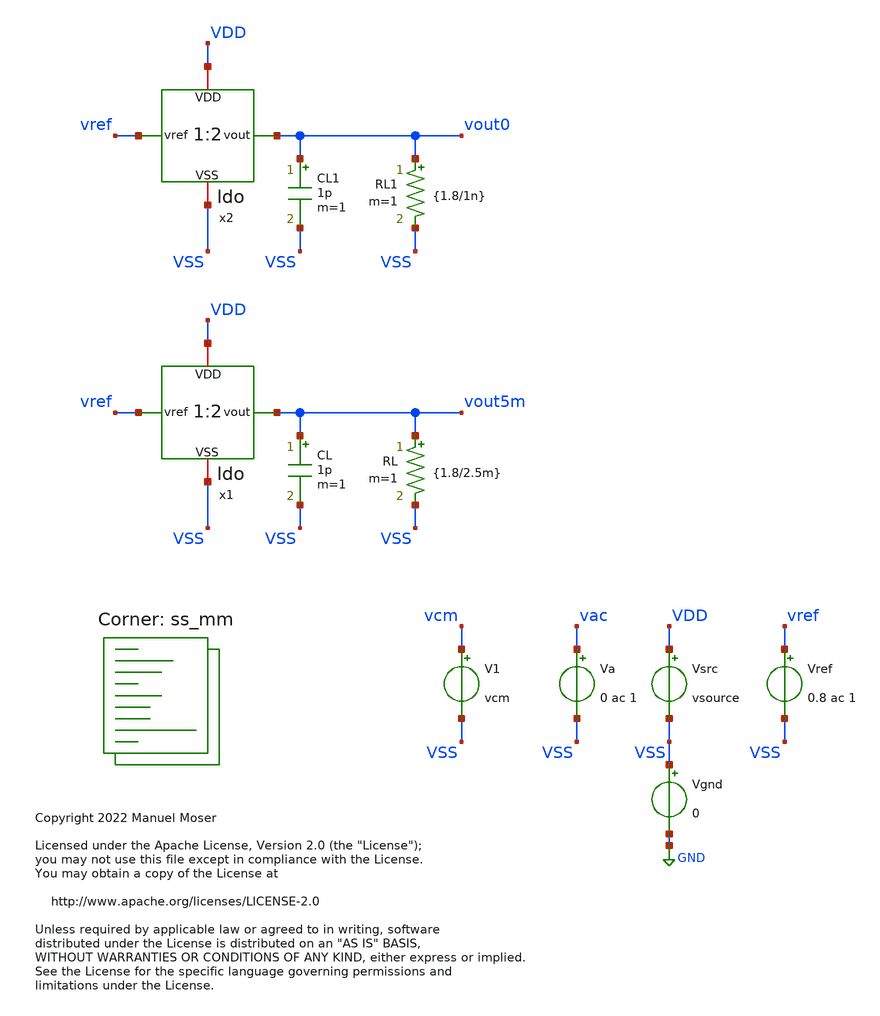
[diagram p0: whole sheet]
** sch_path: xschem/ldo_tb.sch
* Copyright 2022 Manuel Moser
* Licensed under the Apache License, Version 2.0 (the "License");
**.subckt ldo_tb
V1 vcm VSS vcm
Vref vref VSS 0.8 ac 1
Vsrc VDD VSS vsource
Vgnd VSS GND 0
Va vac VSS 0 ac 1
CL vout5m VSS 1p m=1
RL vout5m VSS {1.8/2.5m} m=1
x1 VDD vref vout5m VSS ldo
CL1 vout0 VSS 1p m=1
x2 VDD vref vout0 VSS ldo
RL1 vout0 VSS {1.8/1n} m=1
**** begin user architecture code



.temp 27
.options savecurrents
.option gmin = 1e-18
.option RSHUNT=1E20

.param vsource = 1.8
.param vcm = {vsource/2}


.save all
.control
set num_threads = 12
write results_ldo.raw
set appendwrite

repeat 20
 reset

dc vref 0 1 0.01 temp -30 60 90
write results_ldo.raw vout5m vout0 x1.vota x1.vfb @m.x1.xm5.msky130_fd_pr__nfet_01v8_lvt[id] i(vsrc)

ac dec 10 1 10meg
write results_ldo.raw vout5m


end

.endc




.lib $::SKYWATER_MODELS/sky130.lib.spice ss_mm
**** end user architecture code
**.ends

* expanding   symbol:  ldo.sym # of pins=4
** sym_path: xschem/ldo.sym
** sch_path: xschem/ldo.sch
.subckt ldo VDD vref vout VSS
*.ipin vref
*.iopin VDD
*.iopin VSS
*.opin vout
x1 VDD vref vota vfb VSS ldo_ota
XM1 vout vota VDD VDD sky130_fd_pr__pfet_01v8_hvt L=0.15 W='5 * 10 ' nf=10 ad='int((nf+1)/2) * W / nf * 0.29'
+ as='int((nf+2)/2) * W / nf * 0.29' pd='2*int((nf+1)/2) * (W / nf + 0.29)' ps='2*int((nf+2)/2) * (W / nf + 0.29)'
+ nrd='0.29 / W ' nrs='0.29 / W ' sa=0 sb=0 sd=0 mult=9 m=9
XM5 vout vout net1 net1 sky130_fd_pr__nfet_01v8_lvt L=4 W='2 * 2 ' nf=2 ad='int((nf+1)/2) * W/nf * 0.29'
+ as='int((nf+2)/2) * W/nf * 0.29' pd='2*int((nf+1)/2) * (W/nf + 0.29)' ps='2*int((nf+2)/2) * (W/nf + 0.29)'
+ nrd='0.29 / W' nrs='0.29 / W' sa=0 sb=0 sd=0 mult=1 m=1
XM2 net1 net1 vfb vfb sky130_fd_pr__nfet_01v8_lvt L=4 W='2 * 2 ' nf=2 ad='int((nf+1)/2) * W/nf * 0.29'
+ as='int((nf+2)/2) * W/nf * 0.29' pd='2*int((nf+1)/2) * (W/nf + 0.29)' ps='2*int((nf+2)/2) * (W/nf + 0.29)'
+ nrd='0.29 / W' nrs='0.29 / W' sa=0 sb=0 sd=0 mult=1 m=1
XM3 vfb vfb net2 net2 sky130_fd_pr__nfet_01v8_lvt L=4 W='2 * 2 ' nf=2 ad='int((nf+1)/2) * W/nf * 0.29'
+ as='int((nf+2)/2) * W/nf * 0.29' pd='2*int((nf+1)/2) * (W/nf + 0.29)' ps='2*int((nf+2)/2) * (W/nf + 0.29)'
+ nrd='0.29 / W' nrs='0.29 / W' sa=0 sb=0 sd=0 mult=1 m=1
XM6 net2 net2 VSS VSS sky130_fd_pr__nfet_01v8_lvt L=4 W='2 * 2 ' nf=2 ad='int((nf+1)/2) * W/nf * 0.29'
+ as='int((nf+2)/2) * W/nf * 0.29' pd='2*int((nf+1)/2) * (W/nf + 0.29)' ps='2*int((nf+2)/2) * (W/nf + 0.29)'
+ nrd='0.29 / W' nrs='0.29 / W' sa=0 sb=0 sd=0 mult=1 m=1
.ends


* expanding   symbol:  ldo_ota.sym # of pins=5
** sym_path: xschem/ldo_ota.sym
** sch_path: xschem/ldo_ota.sch
.subckt ldo_ota VDD inp outn inn VSS
*.iopin VDD
*.iopin VSS
*.ipin inp
*.ipin inn
*.opin outn
x2 bias2 VDD VSS bias1 ldo_isource
XM10 net1 bias2 VDD VDD sky130_fd_pr__pfet_01v8_lvt L=8 W='1 * 1 ' nf=1 ad='int((nf+1)/2) * W / nf * 0.29'
+ as='int((nf+2)/2) * W / nf * 0.29' pd='2*int((nf+1)/2) * (W / nf + 0.29)' ps='2*int((nf+2)/2) * (W / nf + 0.29)'
+ nrd='0.29 / W ' nrs='0.29 / W ' sa=0 sb=0 sd=0 mult=1 m=1
XM12 bias2 bias2 net1 VDD sky130_fd_pr__pfet_01v8_lvt L=1 W='3 * 9 ' nf=9 ad='int((nf+1)/2) * W / nf * 0.29'
+ as='int((nf+2)/2) * W / nf * 0.29' pd='2*int((nf+1)/2) * (W / nf + 0.29)' ps='2*int((nf+2)/2) * (W / nf + 0.29)'
+ nrd='0.29 / W ' nrs='0.29 / W ' sa=0 sb=0 sd=0 mult=1 m=1
XM1 net2 bias1 VDD VDD sky130_fd_pr__pfet_01v8_lvt L=8 W='1 * 3 ' nf=3 ad='int((nf+1)/2) * W / nf * 0.29'
+ as='int((nf+2)/2) * W / nf * 0.29' pd='2*int((nf+1)/2) * (W / nf + 0.29)' ps='2*int((nf+2)/2) * (W / nf + 0.29)'
+ nrd='0.29 / W ' nrs='0.29 / W ' sa=0 sb=0 sd=0 mult=1 m=1
XM2 bias1 bias2 net2 VDD sky130_fd_pr__pfet_01v8_lvt L=1 W='3 * 9 ' nf=9 ad='int((nf+1)/2) * W / nf * 0.29'
+ as='int((nf+2)/2) * W / nf * 0.29' pd='2*int((nf+1)/2) * (W / nf + 0.29)' ps='2*int((nf+2)/2) * (W / nf + 0.29)'
+ nrd='0.29 / W ' nrs='0.29 / W ' sa=0 sb=0 sd=0 mult=1 m=1
XM3 net3 bias1 VDD VDD sky130_fd_pr__pfet_01v8_lvt L=8 W='1 * 3 ' nf=3 ad='int((nf+1)/2) * W / nf * 0.29'
+ as='int((nf+2)/2) * W / nf * 0.29' pd='2*int((nf+1)/2) * (W / nf + 0.29)' ps='2*int((nf+2)/2) * (W / nf + 0.29)'
+ nrd='0.29 / W ' nrs='0.29 / W ' sa=0 sb=0 sd=0 mult=1 m=1
XM4 bias3 bias2 net3 VDD sky130_fd_pr__pfet_01v8_lvt L=1 W='3 * 9 ' nf=9 ad='int((nf+1)/2) * W / nf * 0.29'
+ as='int((nf+2)/2) * W / nf * 0.29' pd='2*int((nf+1)/2) * (W / nf + 0.29)' ps='2*int((nf+2)/2) * (W / nf + 0.29)'
+ nrd='0.29 / W ' nrs='0.29 / W ' sa=0 sb=0 sd=0 mult=1 m=1
XM5 net4 bias1 VDD VDD sky130_fd_pr__pfet_01v8_lvt L=8 W='1 * 3 ' nf=3 ad='int((nf+1)/2) * W / nf * 0.29'
+ as='int((nf+2)/2) * W / nf * 0.29' pd='2*int((nf+1)/2) * (W / nf + 0.29)' ps='2*int((nf+2)/2) * (W / nf + 0.29)'
+ nrd='0.29 / W ' nrs='0.29 / W ' sa=0 sb=0 sd=0 mult=1 m=1
XM8 bias4 bias2 net4 VDD sky130_fd_pr__pfet_01v8_lvt L=1 W='3 * 9 ' nf=9 ad='int((nf+1)/2) * W / nf * 0.29'
+ as='int((nf+2)/2) * W / nf * 0.29' pd='2*int((nf+1)/2) * (W / nf + 0.29)' ps='2*int((nf+2)/2) * (W / nf + 0.29)'
+ nrd='0.29 / W ' nrs='0.29 / W ' sa=0 sb=0 sd=0 mult=1 m=1
XM9 bias3 bias3 net5 VSS sky130_fd_pr__nfet_01v8_lvt L=4 W='1 * 9 ' nf=9 ad='int((nf+1)/2) * W / nf * 0.29'
+ as='int((nf+2)/2) * W / nf * 0.29' pd='2*int((nf+1)/2) * (W / nf + 0.29)' ps='2*int((nf+2)/2) * (W / nf + 0.29)'
+ nrd='0.29 / W ' nrs='0.29 / W ' sa=0 sb=0 sd=0 mult=1 m=1
XM11 net5 bias3 net10 VSS sky130_fd_pr__nfet_01v8_lvt L=4 W='1 * 1 ' nf=1 ad='int((nf+1)/2) * W / nf * 0.29'
+ as='int((nf+2)/2) * W / nf * 0.29' pd='2*int((nf+1)/2) * (W / nf + 0.29)' ps='2*int((nf+2)/2) * (W / nf + 0.29)'
+ nrd='0.29 / W ' nrs='0.29 / W ' sa=0 sb=0 sd=0 mult=1 m=1
XM13 bias4 bias3 net6 VSS sky130_fd_pr__nfet_01v8_lvt L=4 W='1 * 9 ' nf=9 ad='int((nf+1)/2) * W / nf * 0.29'
+ as='int((nf+2)/2) * W / nf * 0.29' pd='2*int((nf+1)/2) * (W / nf + 0.29)' ps='2*int((nf+2)/2) * (W / nf + 0.29)'
+ nrd='0.29 / W ' nrs='0.29 / W ' sa=0 sb=0 sd=0 mult=1 m=1
XM14 net6 bias4 net7 VSS sky130_fd_pr__nfet_01v8_lvt L=4 W='1 * 3 ' nf=3 ad='int((nf+1)/2) * W / nf * 0.29'
+ as='int((nf+2)/2) * W / nf * 0.29' pd='2*int((nf+1)/2) * (W / nf + 0.29)' ps='2*int((nf+2)/2) * (W / nf + 0.29)'
+ nrd='0.29 / W ' nrs='0.29 / W ' sa=0 sb=0 sd=0 mult=1 m=1
XM6 net7 bias4 net8 VSS sky130_fd_pr__nfet_01v8_lvt L=4 W='1 * 3 ' nf=3 ad='int((nf+1)/2) * W / nf * 0.29'
+ as='int((nf+2)/2) * W / nf * 0.29' pd='2*int((nf+1)/2) * (W / nf + 0.29)' ps='2*int((nf+2)/2) * (W / nf + 0.29)'
+ nrd='0.29 / W ' nrs='0.29 / W ' sa=0 sb=0 sd=0 mult=1 m=1
XM7 net10 bias3 net9 VSS sky130_fd_pr__nfet_01v8_lvt L=4 W='1 * 1 ' nf=1 ad='int((nf+1)/2) * W / nf * 0.29'
+ as='int((nf+2)/2) * W / nf * 0.29' pd='2*int((nf+1)/2) * (W / nf + 0.29)' ps='2*int((nf+2)/2) * (W / nf + 0.29)'
+ nrd='0.29 / W ' nrs='0.29 / W ' sa=0 sb=0 sd=0 mult=1 m=1
XM15 net8 bias4 VSS VSS sky130_fd_pr__nfet_01v8_lvt L=4 W='1 * 3 ' nf=3 ad='int((nf+1)/2) * W / nf * 0.29'
+ as='int((nf+2)/2) * W / nf * 0.29' pd='2*int((nf+1)/2) * (W / nf + 0.29)' ps='2*int((nf+2)/2) * (W / nf + 0.29)'
+ nrd='0.29 / W ' nrs='0.29 / W ' sa=0 sb=0 sd=0 mult=1 m=1
XM16 net9 bias3 VSS VSS sky130_fd_pr__nfet_01v8_lvt L=4 W='1 * 1 ' nf=1 ad='int((nf+1)/2) * W / nf * 0.29'
+ as='int((nf+2)/2) * W / nf * 0.29' pd='2*int((nf+1)/2) * (W / nf + 0.29)' ps='2*int((nf+2)/2) * (W / nf + 0.29)'
+ nrd='0.29 / W ' nrs='0.29 / W ' sa=0 sb=0 sd=0 mult=1 m=1
x1 VDD inp inn bias1 bias2 bias3 outn VSS bias4 ldo_fc_n
.ends


* expanding   symbol:  ldo_isource.sym # of pins=4
** sym_path: xschem/ldo_isource.sym
** sch_path: xschem/ldo_isource.sch
.subckt ldo_isource curr_n1 VDD VSS curr_n2
*.iopin VDD
*.iopin VSS
*.ipin curr_n1
*.ipin curr_n2
XMP2 VGP VGP net4 VDD sky130_fd_pr__pfet_01v8_lvt L=8 W='0.55 * 7 ' nf=7 ad='int((nf+1)/2) * W / nf * 0.29'
+ as='int((nf+2)/2) * W / nf * 0.29' pd='2*int((nf+1)/2) * (W / nf + 0.29)' ps='2*int((nf+2)/2) * (W / nf + 0.29)'
+ nrd='0.29 / W ' nrs='0.29 / W ' sa=0 sb=0 sd=0 mult=1 m=1
XMP1 VGN VGP net3 VDD sky130_fd_pr__pfet_01v8_lvt L=8 W='0.55 * 7 ' nf=7 ad='int((nf+1)/2) * W / nf * 0.29'
+ as='int((nf+2)/2) * W / nf * 0.29' pd='2*int((nf+1)/2) * (W / nf + 0.29)' ps='2*int((nf+2)/2) * (W / nf + 0.29)'
+ nrd='0.29 / W ' nrs='0.29 / W ' sa=0 sb=0 sd=0 mult=1 m=1
XMN1 VGN VGN net1 VSS sky130_fd_pr__nfet_01v8_lvt L=8 W='7 * 1 ' nf=1 ad='int((nf+1)/2) * W / nf * 0.29'
+ as='int((nf+2)/2) * W / nf * 0.29' pd='2*int((nf+1)/2) * (W / nf + 0.29)' ps='2*int((nf+2)/2) * (W / nf + 0.29)'
+ nrd='0.29 / W ' nrs='0.29 / W ' sa=0 sb=0 sd=0 mult=1 m=1
XMN2 VGP VGN net2 VSS sky130_fd_pr__nfet_01v8_lvt L=8 W='7 * 1 ' nf=1 ad='int((nf+1)/2) * W / nf * 0.29'
+ as='int((nf+2)/2) * W / nf * 0.29' pd='2*int((nf+1)/2) * (W / nf + 0.29)' ps='2*int((nf+2)/2) * (W / nf + 0.29)'
+ nrd='0.29 / W ' nrs='0.29 / W ' sa=0 sb=0 sd=0 mult=5 m=5
XMN3 net1 VGN VSS VSS sky130_fd_pr__nfet_01v8_lvt L=8 W='7 * 1 ' nf=1 ad='int((nf+1)/2) * W / nf * 0.29'
+ as='int((nf+2)/2) * W / nf * 0.29' pd='2*int((nf+1)/2) * (W / nf + 0.29)' ps='2*int((nf+2)/2) * (W / nf + 0.29)'
+ nrd='0.29 / W ' nrs='0.29 / W ' sa=0 sb=0 sd=0 mult=1 m=1
XMN4 net2 VGN Vref VSS sky130_fd_pr__nfet_01v8_lvt L=8 W='7 * 1 ' nf=1 ad='int((nf+1)/2) * W / nf * 0.29'
+ as='int((nf+2)/2) * W / nf * 0.29' pd='2*int((nf+1)/2) * (W / nf + 0.29)' ps='2*int((nf+2)/2) * (W / nf + 0.29)'
+ nrd='0.29 / W ' nrs='0.29 / W ' sa=0 sb=0 sd=0 mult=5 m=5
XMP4 net3 VGP VDD VDD sky130_fd_pr__pfet_01v8_lvt L=8 W='0.55 * 7 ' nf=7 ad='int((nf+1)/2) * W / nf * 0.29'
+ as='int((nf+2)/2) * W / nf * 0.29' pd='2*int((nf+1)/2) * (W / nf + 0.29)' ps='2*int((nf+2)/2) * (W / nf + 0.29)'
+ nrd='0.29 / W ' nrs='0.29 / W ' sa=0 sb=0 sd=0 mult=1 m=1
XMP5 net4 VGP VDD VDD sky130_fd_pr__pfet_01v8_lvt L=8 W='0.55 * 7 ' nf=7 ad='int((nf+1)/2) * W / nf * 0.29'
+ as='int((nf+2)/2) * W / nf * 0.29' pd='2*int((nf+1)/2) * (W / nf + 0.29)' ps='2*int((nf+2)/2) * (W / nf + 0.29)'
+ nrd='0.29 / W ' nrs='0.29 / W ' sa=0 sb=0 sd=0 mult=1 m=1
XMP3 Vrefgate VGP net19 VDD sky130_fd_pr__pfet_01v8_lvt L=8 W='0.55 * 7 ' nf=7 ad='int((nf+1)/2) * W / nf * 0.29'
+ as='int((nf+2)/2) * W / nf * 0.29' pd='2*int((nf+1)/2) * (W / nf + 0.29)' ps='2*int((nf+2)/2) * (W / nf + 0.29)'
+ nrd='0.29 / W ' nrs='0.29 / W ' sa=0 sb=0 sd=0 mult=1 m=1
XM2 net5 Vrefgate net6 VSS sky130_fd_pr__nfet_01v8 L=4 W='1 * 1 ' nf=1 ad='int((nf+1)/2) * W / nf * 0.29'
+ as='int((nf+2)/2) * W / nf * 0.29' pd='2*int((nf+1)/2) * (W / nf + 0.29)' ps='2*int((nf+2)/2) * (W / nf + 0.29)'
+ nrd='0.29 / W ' nrs='0.29 / W ' sa=0 sb=0 sd=0 mult=1 m=1
XM3 net8 Vrefgate VSS VSS sky130_fd_pr__nfet_01v8 L=4 W='1 * 1 ' nf=1 ad='int((nf+1)/2) * W / nf * 0.29'
+ as='int((nf+2)/2) * W / nf * 0.29' pd='2*int((nf+1)/2) * (W / nf + 0.29)' ps='2*int((nf+2)/2) * (W / nf + 0.29)'
+ nrd='0.29 / W ' nrs='0.29 / W ' sa=0 sb=0 sd=0 mult=1 m=1
XM1 net7 Vrefgate net8 VSS sky130_fd_pr__nfet_01v8 L=4 W='1 * 1 ' nf=1 ad='int((nf+1)/2) * W / nf * 0.29'
+ as='int((nf+2)/2) * W / nf * 0.29' pd='2*int((nf+1)/2) * (W / nf + 0.29)' ps='2*int((nf+2)/2) * (W / nf + 0.29)'
+ nrd='0.29 / W ' nrs='0.29 / W ' sa=0 sb=0 sd=0 mult=1 m=1
XM4 net6 Vrefgate net7 VSS sky130_fd_pr__nfet_01v8 L=4 W='1 * 1 ' nf=1 ad='int((nf+1)/2) * W / nf * 0.29'
+ as='int((nf+2)/2) * W / nf * 0.29' pd='2*int((nf+1)/2) * (W / nf + 0.29)' ps='2*int((nf+2)/2) * (W / nf + 0.29)'
+ nrd='0.29 / W ' nrs='0.29 / W ' sa=0 sb=0 sd=0 mult=1 m=1
XMN5 net10 Vrefgate VSS VSS sky130_fd_pr__nfet_01v8_lvt L=4 W='1 * 1 ' nf=1 ad='int((nf+1)/2) * W / nf * 0.29'
+ as='int((nf+2)/2) * W / nf * 0.29' pd='2*int((nf+1)/2) * (W / nf + 0.29)' ps='2*int((nf+2)/2) * (W / nf + 0.29)'
+ nrd='0.29 / W ' nrs='0.29 / W ' sa=0 sb=0 sd=0 mult=1 m=1
XMN6 net14 Vrefgate net9 VSS sky130_fd_pr__nfet_01v8_lvt L=4 W='1 * 1 ' nf=1 ad='int((nf+1)/2) * W / nf * 0.29'
+ as='int((nf+2)/2) * W / nf * 0.29' pd='2*int((nf+1)/2) * (W / nf + 0.29)' ps='2*int((nf+2)/2) * (W / nf + 0.29)'
+ nrd='0.29 / W ' nrs='0.29 / W ' sa=0 sb=0 sd=0 mult=1 m=1
XMN9 net16 Vrefgate net14 VSS sky130_fd_pr__nfet_01v8_lvt L=4 W='1 * 1 ' nf=1 ad='int((nf+1)/2) * W / nf * 0.29'
+ as='int((nf+2)/2) * W / nf * 0.29' pd='2*int((nf+1)/2) * (W / nf + 0.29)' ps='2*int((nf+2)/2) * (W / nf + 0.29)'
+ nrd='0.29 / W ' nrs='0.29 / W ' sa=0 sb=0 sd=0 mult=1 m=1
XM5 Vrefgate Vrefgate net5 VSS sky130_fd_pr__nfet_01v8 L=4 W='1 * 1 ' nf=1 ad='int((nf+1)/2) * W / nf * 0.29'
+ as='int((nf+2)/2) * W / nf * 0.29' pd='2*int((nf+1)/2) * (W / nf + 0.29)' ps='2*int((nf+2)/2) * (W / nf + 0.29)'
+ nrd='0.29 / W ' nrs='0.29 / W ' sa=0 sb=0 sd=0 mult=1 m=1
XMN10 net11 Vrefgate net10 VSS sky130_fd_pr__nfet_01v8_lvt L=4 W='1 * 1 ' nf=1 ad='int((nf+1)/2) * W / nf * 0.29'
+ as='int((nf+2)/2) * W / nf * 0.29' pd='2*int((nf+1)/2) * (W / nf + 0.29)' ps='2*int((nf+2)/2) * (W / nf + 0.29)'
+ nrd='0.29 / W ' nrs='0.29 / W ' sa=0 sb=0 sd=0 mult=1 m=1
XMN11 net12 Vrefgate net11 VSS sky130_fd_pr__nfet_01v8_lvt L=4 W='1 * 1 ' nf=1 ad='int((nf+1)/2) * W / nf * 0.29'
+ as='int((nf+2)/2) * W / nf * 0.29' pd='2*int((nf+1)/2) * (W / nf + 0.29)' ps='2*int((nf+2)/2) * (W / nf + 0.29)'
+ nrd='0.29 / W ' nrs='0.29 / W ' sa=0 sb=0 sd=0 mult=1 m=1
XMN12 net13 Vrefgate net12 VSS sky130_fd_pr__nfet_01v8_lvt L=4 W='1 * 1 ' nf=1 ad='int((nf+1)/2) * W / nf * 0.29'
+ as='int((nf+2)/2) * W / nf * 0.29' pd='2*int((nf+1)/2) * (W / nf + 0.29)' ps='2*int((nf+2)/2) * (W / nf + 0.29)'
+ nrd='0.29 / W ' nrs='0.29 / W ' sa=0 sb=0 sd=0 mult=1 m=1
XMN13 net9 Vrefgate net13 VSS sky130_fd_pr__nfet_01v8_lvt L=4 W='1 * 1 ' nf=1 ad='int((nf+1)/2) * W / nf * 0.29'
+ as='int((nf+2)/2) * W / nf * 0.29' pd='2*int((nf+1)/2) * (W / nf + 0.29)' ps='2*int((nf+2)/2) * (W / nf + 0.29)'
+ nrd='0.29 / W ' nrs='0.29 / W ' sa=0 sb=0 sd=0 mult=1 m=1
XMN7 net18 Vrefgate net15 VSS sky130_fd_pr__nfet_01v8_lvt L=4 W='1 * 1 ' nf=1 ad='int((nf+1)/2) * W / nf * 0.29'
+ as='int((nf+2)/2) * W / nf * 0.29' pd='2*int((nf+1)/2) * (W / nf + 0.29)' ps='2*int((nf+2)/2) * (W / nf + 0.29)'
+ nrd='0.29 / W ' nrs='0.29 / W ' sa=0 sb=0 sd=0 mult=1 m=1
XMN8 Vref Vrefgate net18 VSS sky130_fd_pr__nfet_01v8_lvt L=4 W='1 * 1 ' nf=1 ad='int((nf+1)/2) * W / nf * 0.29'
+ as='int((nf+2)/2) * W / nf * 0.29' pd='2*int((nf+1)/2) * (W / nf + 0.29)' ps='2*int((nf+2)/2) * (W / nf + 0.29)'
+ nrd='0.29 / W ' nrs='0.29 / W ' sa=0 sb=0 sd=0 mult=1 m=1
XMN14 net17 Vrefgate net16 VSS sky130_fd_pr__nfet_01v8_lvt L=4 W='1 * 1 ' nf=1 ad='int((nf+1)/2) * W / nf * 0.29'
+ as='int((nf+2)/2) * W / nf * 0.29' pd='2*int((nf+1)/2) * (W / nf + 0.29)' ps='2*int((nf+2)/2) * (W / nf + 0.29)'
+ nrd='0.29 / W ' nrs='0.29 / W ' sa=0 sb=0 sd=0 mult=1 m=1
XMN15 net15 Vrefgate net17 VSS sky130_fd_pr__nfet_01v8_lvt L=4 W='1 * 1 ' nf=1 ad='int((nf+1)/2) * W / nf * 0.29'
+ as='int((nf+2)/2) * W / nf * 0.29' pd='2*int((nf+1)/2) * (W / nf + 0.29)' ps='2*int((nf+2)/2) * (W / nf + 0.29)'
+ nrd='0.29 / W ' nrs='0.29 / W ' sa=0 sb=0 sd=0 mult=1 m=1
XMP6 net19 VGP VDD VDD sky130_fd_pr__pfet_01v8_lvt L=8 W='0.55 * 7 ' nf=7 ad='int((nf+1)/2) * W / nf * 0.29'
+ as='int((nf+2)/2) * W / nf * 0.29' pd='2*int((nf+1)/2) * (W / nf + 0.29)' ps='2*int((nf+2)/2) * (W / nf + 0.29)'
+ nrd='0.29 / W ' nrs='0.29 / W ' sa=0 sb=0 sd=0 mult=1 m=1
XMN16 curr_n1 VGN net20 VSS sky130_fd_pr__nfet_01v8_lvt L=8 W='7 * 1 ' nf=1 ad='int((nf+1)/2) * W / nf * 0.29'
+ as='int((nf+2)/2) * W / nf * 0.29' pd='2*int((nf+1)/2) * (W / nf + 0.29)' ps='2*int((nf+2)/2) * (W / nf + 0.29)'
+ nrd='0.29 / W ' nrs='0.29 / W ' sa=0 sb=0 sd=0 mult=1 m=1
XMN17 net20 VGN VSS VSS sky130_fd_pr__nfet_01v8_lvt L=8 W='7 * 1 ' nf=1 ad='int((nf+1)/2) * W / nf * 0.29'
+ as='int((nf+2)/2) * W / nf * 0.29' pd='2*int((nf+1)/2) * (W / nf + 0.29)' ps='2*int((nf+2)/2) * (W / nf + 0.29)'
+ nrd='0.29 / W ' nrs='0.29 / W ' sa=0 sb=0 sd=0 mult=1 m=1
XM6 VGP net21 VGN VSS sky130_fd_pr__nfet_01v8 L=4 W='1 * 1 ' nf=1 ad='int((nf+1)/2) * W / nf * 0.29'
+ as='int((nf+2)/2) * W / nf * 0.29' pd='2*int((nf+1)/2) * (W / nf + 0.29)' ps='2*int((nf+2)/2) * (W / nf + 0.29)'
+ nrd='0.29 / W ' nrs='0.29 / W ' sa=0 sb=0 sd=0 mult=1 m=1
XM7 net21 Vrefgate VSS VSS sky130_fd_pr__nfet_01v8 L=4 W='1 * 1 ' nf=1 ad='int((nf+1)/2) * W / nf * 0.29'
+ as='int((nf+2)/2) * W / nf * 0.29' pd='2*int((nf+1)/2) * (W / nf + 0.29)' ps='2*int((nf+2)/2) * (W / nf + 0.29)'
+ nrd='0.29 / W ' nrs='0.29 / W ' sa=0 sb=0 sd=0 mult=1 m=1
XC1 VDD net21 VSS sky130_fd_pr__cap_var_lvt W=2 L=2 VM=1 m=1
XMN18 curr_n2 VGN net22 VSS sky130_fd_pr__nfet_01v8_lvt L=8 W='7 * 1 ' nf=1 ad='int((nf+1)/2) * W / nf * 0.29'
+ as='int((nf+2)/2) * W / nf * 0.29' pd='2*int((nf+1)/2) * (W / nf + 0.29)' ps='2*int((nf+2)/2) * (W / nf + 0.29)'
+ nrd='0.29 / W ' nrs='0.29 / W ' sa=0 sb=0 sd=0 mult=1 m=1
XMN19 net22 VGN VSS VSS sky130_fd_pr__nfet_01v8_lvt L=8 W='7 * 1 ' nf=1 ad='int((nf+1)/2) * W / nf * 0.29'
+ as='int((nf+2)/2) * W / nf * 0.29' pd='2*int((nf+1)/2) * (W / nf + 0.29)' ps='2*int((nf+2)/2) * (W / nf + 0.29)'
+ nrd='0.29 / W ' nrs='0.29 / W ' sa=0 sb=0 sd=0 mult=1 m=1
.ends


* expanding   symbol:  ldo_fc_n.sym # of pins=9
** sym_path: xschem/ldo_fc_n.sym
** sch_path: xschem/ldo_fc_n.sch
.subckt ldo_fc_n VDD inp inn bias1 bias2 bias3 outn VSS bias4
*.iopin VSS
*.iopin VDD
*.ipin inp
*.ipin inn
*.ipin bias1
*.opin outn
*.ipin bias2
*.ipin bias3
*.ipin bias4
XMN4 outn bias3 net1 VSS sky130_fd_pr__nfet_01v8_lvt L=4 W='1 * 9 ' nf=9 ad='int((nf+1)/2) * W / nf * 0.29'
+ as='int((nf+2)/2) * W / nf * 0.29' pd='2*int((nf+1)/2) * (W / nf + 0.29)' ps='2*int((nf+2)/2) * (W / nf + 0.29)'
+ nrd='0.29 / W ' nrs='0.29 / W ' sa=0 sb=0 sd=0 mult=12 m=12
XMN7 net1 net3 net8 VSS sky130_fd_pr__nfet_01v8_lvt L=4 W='1 * 3 ' nf=3 ad='int((nf+1)/2) * W / nf * 0.29'
+ as='int((nf+2)/2) * W / nf * 0.29' pd='2*int((nf+1)/2) * (W / nf + 0.29)' ps='2*int((nf+2)/2) * (W / nf + 0.29)'
+ nrd='0.29 / W ' nrs='0.29 / W ' sa=0 sb=0 sd=0 mult=12 m=12
XMN3 net3 bias3 net2 VSS sky130_fd_pr__nfet_01v8_lvt L=4 W='1 * 9 ' nf=9 ad='int((nf+1)/2) * W / nf * 0.29'
+ as='int((nf+2)/2) * W / nf * 0.29' pd='2*int((nf+1)/2) * (W / nf + 0.29)' ps='2*int((nf+2)/2) * (W / nf + 0.29)'
+ nrd='0.29 / W ' nrs='0.29 / W ' sa=0 sb=0 sd=0 mult=12 m=12
XMN6 net2 net3 net7 VSS sky130_fd_pr__nfet_01v8_lvt L=4 W='1 * 3 ' nf=3 ad='int((nf+1)/2) * W / nf * 0.29'
+ as='int((nf+2)/2) * W / nf * 0.29' pd='2*int((nf+1)/2) * (W / nf + 0.29)' ps='2*int((nf+2)/2) * (W / nf + 0.29)'
+ nrd='0.29 / W ' nrs='0.29 / W ' sa=0 sb=0 sd=0 mult=12 m=12
XMP4 outn bias2 net5 VDD sky130_fd_pr__pfet_01v8_lvt L=1 W='3 * 9 ' nf=9 ad='int((nf+1)/2) * W / nf * 0.29'
+ as='int((nf+2)/2) * W / nf * 0.29' pd='2*int((nf+1)/2) * (W / nf + 0.29)' ps='2*int((nf+2)/2) * (W / nf + 0.29)'
+ nrd='0.29 / W ' nrs='0.29 / W ' sa=0 sb=0 sd=0 mult=12 m=12
XMP2 net5 bias1 VDD VDD sky130_fd_pr__pfet_01v8_lvt L=8 W='1 * 3 ' nf=3 ad='int((nf+1)/2) * W / nf * 0.29'
+ as='int((nf+2)/2) * W / nf * 0.29' pd='2*int((nf+1)/2) * (W / nf + 0.29)' ps='2*int((nf+2)/2) * (W / nf + 0.29)'
+ nrd='0.29 / W ' nrs='0.29 / W ' sa=0 sb=0 sd=0 mult=19 m=19
XMP3 net3 bias2 net4 VDD sky130_fd_pr__pfet_01v8_lvt L=1 W='3 * 9 ' nf=9 ad='int((nf+1)/2) * W / nf * 0.29'
+ as='int((nf+2)/2) * W / nf * 0.29' pd='2*int((nf+1)/2) * (W / nf + 0.29)' ps='2*int((nf+2)/2) * (W / nf + 0.29)'
+ nrd='0.29 / W ' nrs='0.29 / W ' sa=0 sb=0 sd=0 mult=12 m=12
XMP1 net4 bias1 VDD VDD sky130_fd_pr__pfet_01v8_lvt L=8 W='1 * 3 ' nf=3 ad='int((nf+1)/2) * W / nf * 0.29'
+ as='int((nf+2)/2) * W / nf * 0.29' pd='2*int((nf+1)/2) * (W / nf + 0.29)' ps='2*int((nf+2)/2) * (W / nf + 0.29)'
+ nrd='0.29 / W ' nrs='0.29 / W ' sa=0 sb=0 sd=0 mult=19 m=19
XMN5 net6 bias4 net9 VSS sky130_fd_pr__nfet_01v8_lvt L=4 W='1 * 3 ' nf=3 ad='int((nf+1)/2) * W / nf * 0.29'
+ as='int((nf+2)/2) * W / nf * 0.29' pd='2*int((nf+1)/2) * (W / nf + 0.29)' ps='2*int((nf+2)/2) * (W / nf + 0.29)'
+ nrd='0.29 / W ' nrs='0.29 / W ' sa=0 sb=0 sd=0 mult=14 m=14
XMN1 net4 inn net6 VSS sky130_fd_pr__nfet_01v8_lvt L=0.25 W='7 * 5 ' nf=5 ad='int((nf+1)/2) * W / nf * 0.29'
+ as='int((nf+2)/2) * W / nf * 0.29' pd='2*int((nf+1)/2) * (W / nf + 0.29)' ps='2*int((nf+2)/2) * (W / nf + 0.29)'
+ nrd='0.29 / W ' nrs='0.29 / W ' sa=0 sb=0 sd=0 mult=1 m=1
XMN2 net5 inp net6 VSS sky130_fd_pr__nfet_01v8_lvt L=0.25 W='7 * 5 ' nf=5 ad='int((nf+1)/2) * W / nf * 0.29'
+ as='int((nf+2)/2) * W / nf * 0.29' pd='2*int((nf+1)/2) * (W / nf + 0.29)' ps='2*int((nf+2)/2) * (W / nf + 0.29)'
+ nrd='0.29 / W ' nrs='0.29 / W ' sa=0 sb=0 sd=0 mult=1 m=1
XMN9 net8 net3 net10 VSS sky130_fd_pr__nfet_01v8_lvt L=4 W='1 * 3 ' nf=3 ad='int((nf+1)/2) * W / nf * 0.29'
+ as='int((nf+2)/2) * W / nf * 0.29' pd='2*int((nf+1)/2) * (W / nf + 0.29)' ps='2*int((nf+2)/2) * (W / nf + 0.29)'
+ nrd='0.29 / W ' nrs='0.29 / W ' sa=0 sb=0 sd=0 mult=12 m=12
XMN10 net7 net3 net11 VSS sky130_fd_pr__nfet_01v8_lvt L=4 W='1 * 3 ' nf=3 ad='int((nf+1)/2) * W / nf * 0.29'
+ as='int((nf+2)/2) * W / nf * 0.29' pd='2*int((nf+1)/2) * (W / nf + 0.29)' ps='2*int((nf+2)/2) * (W / nf + 0.29)'
+ nrd='0.29 / W ' nrs='0.29 / W ' sa=0 sb=0 sd=0 mult=12 m=12
XMN11 net9 bias4 net12 VSS sky130_fd_pr__nfet_01v8_lvt L=4 W='1 * 3 ' nf=3 ad='int((nf+1)/2) * W / nf * 0.29'
+ as='int((nf+2)/2) * W / nf * 0.29' pd='2*int((nf+1)/2) * (W / nf + 0.29)' ps='2*int((nf+2)/2) * (W / nf + 0.29)'
+ nrd='0.29 / W ' nrs='0.29 / W ' sa=0 sb=0 sd=0 mult=14 m=14
XMN8 net10 net3 VSS VSS sky130_fd_pr__nfet_01v8_lvt L=4 W='1 * 3 ' nf=3 ad='int((nf+1)/2) * W / nf * 0.29'
+ as='int((nf+2)/2) * W / nf * 0.29' pd='2*int((nf+1)/2) * (W / nf + 0.29)' ps='2*int((nf+2)/2) * (W / nf + 0.29)'
+ nrd='0.29 / W ' nrs='0.29 / W ' sa=0 sb=0 sd=0 mult=12 m=12
XMN12 net11 net3 VSS VSS sky130_fd_pr__nfet_01v8_lvt L=4 W='1 * 3 ' nf=3 ad='int((nf+1)/2) * W / nf * 0.29'
+ as='int((nf+2)/2) * W / nf * 0.29' pd='2*int((nf+1)/2) * (W / nf + 0.29)' ps='2*int((nf+2)/2) * (W / nf + 0.29)'
+ nrd='0.29 / W ' nrs='0.29 / W ' sa=0 sb=0 sd=0 mult=12 m=12
XMN13 net12 bias4 VSS VSS sky130_fd_pr__nfet_01v8_lvt L=4 W='1 * 3 ' nf=3 ad='int((nf+1)/2) * W / nf * 0.29'
+ as='int((nf+2)/2) * W / nf * 0.29' pd='2*int((nf+1)/2) * (W / nf + 0.29)' ps='2*int((nf+2)/2) * (W / nf + 0.29)'
+ nrd='0.29 / W ' nrs='0.29 / W ' sa=0 sb=0 sd=0 mult=14 m=14
.ends

.GLOBAL GND
.end
